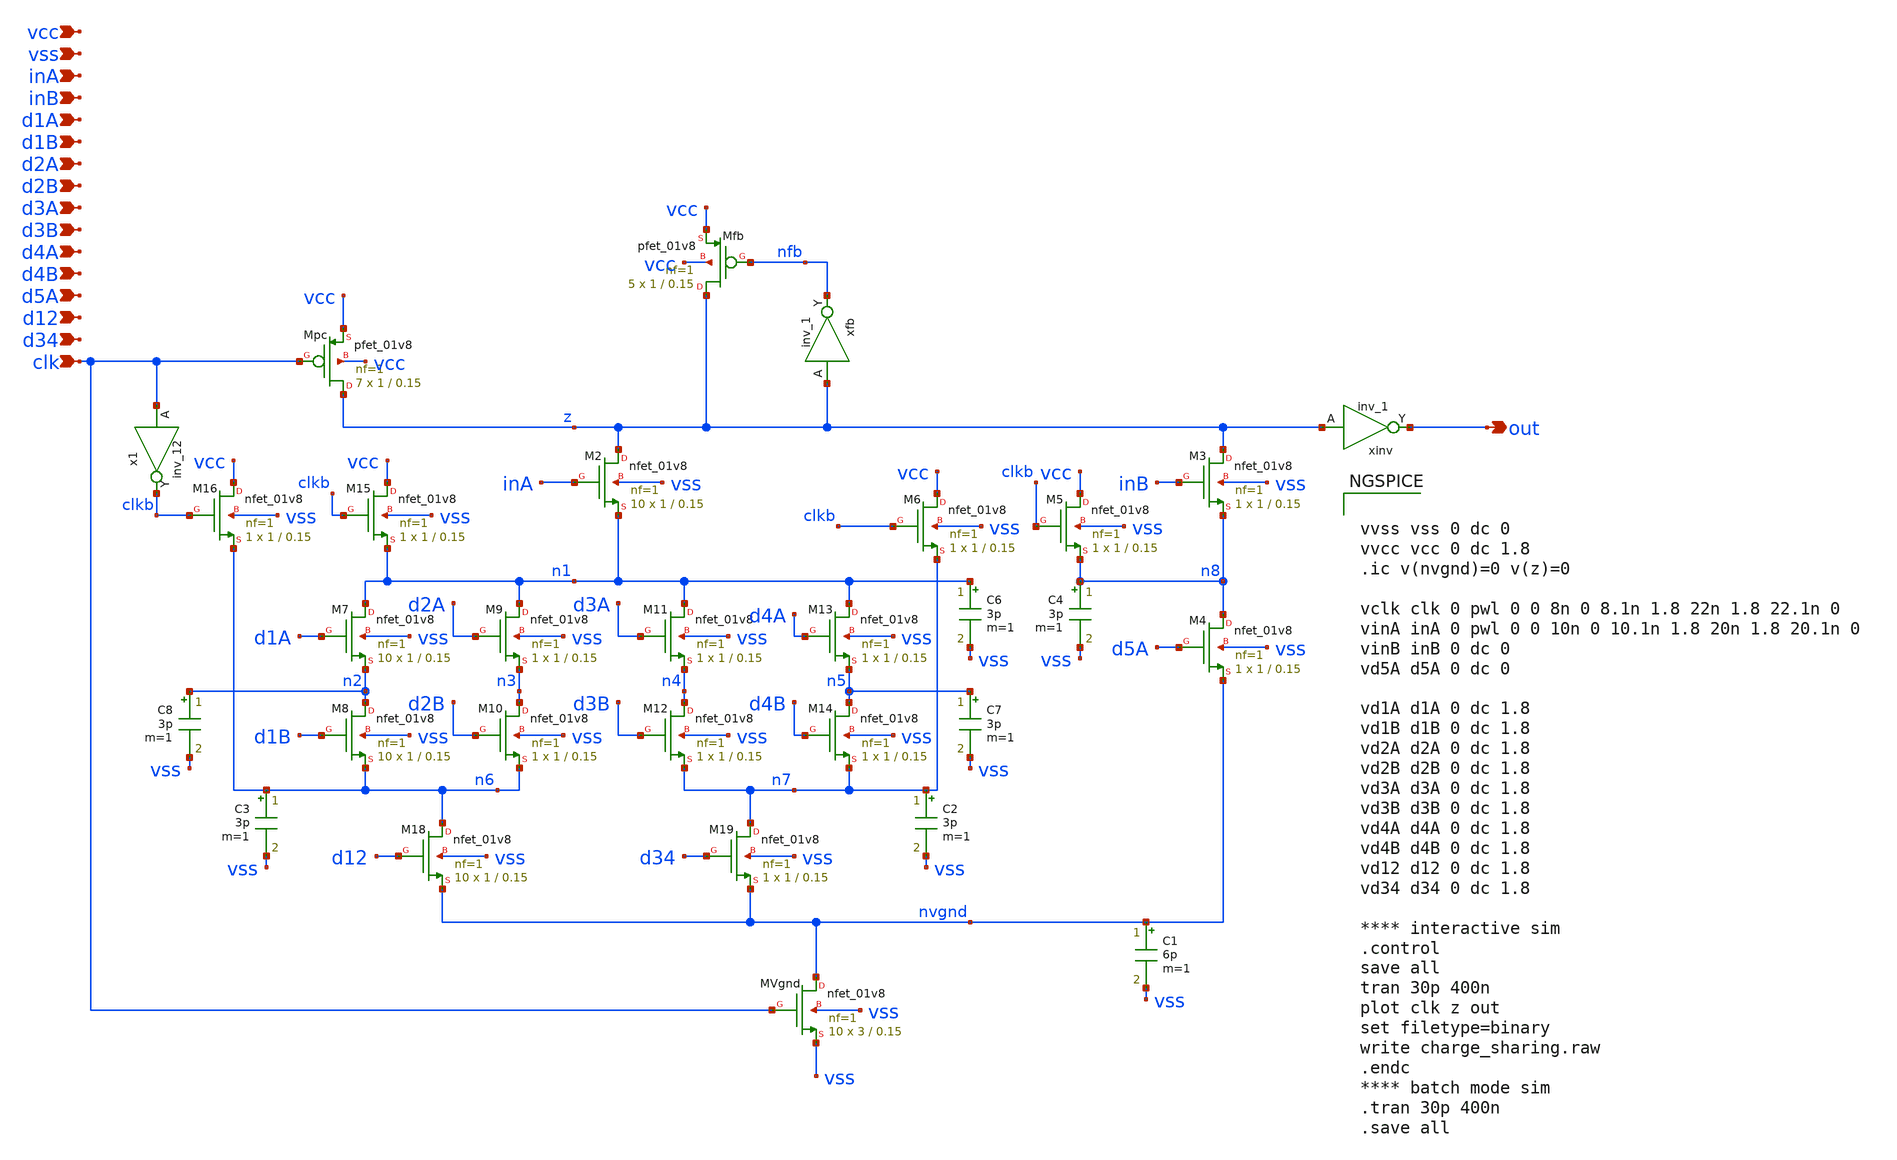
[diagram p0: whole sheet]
** sch_path: src/xe/test_cases/charge_sharing.sch
**.subckt charge_sharing clk out d5A d4B d4A d3B d3A d2B d2A d1B d1A inB inA d34 d12 vss vcc
*.ipin clk
*.opin out
*.ipin d5A
*.ipin d4B
*.ipin d4A
*.ipin d3B
*.ipin d3A
*.ipin d2B
*.ipin d2A
*.ipin d1B
*.ipin d1A
*.ipin inB
*.ipin inA
*.ipin d34
*.ipin d12
*.ipin vss
*.ipin vcc
XMpc z clk vcc vcc sky130_fd_pr__pfet_01v8 L=0.15 W=1 nf=1 ad='int((nf+1)/2) * W/nf * 0.29' as='int((nf+2)/2) * W/nf * 0.29'
+ pd='2*int((nf+1)/2) * (W/nf + 0.29)' ps='2*int((nf+2)/2) * (W/nf + 0.29)' nrd='0.29 / W' nrs='0.29 / W'
+ sa=0 sb=0 sd=0 mult=7 m=7
XM2 z inA n1 vss sky130_fd_pr__nfet_01v8 L=0.15 W=1 nf=1 ad='int((nf+1)/2) * W/nf * 0.29' as='int((nf+2)/2) * W/nf * 0.29'
+ pd='2*int((nf+1)/2) * (W/nf + 0.29)' ps='2*int((nf+2)/2) * (W/nf + 0.29)' nrd='0.29 / W' nrs='0.29 / W'
+ sa=0 sb=0 sd=0 mult=10 m=10
xfb z vss vss vcc vcc nfb sky130_fd_sc_hd__inv_1
xinv z vss vss vcc vcc out sky130_fd_sc_hd__inv_1
XM3 z inB n8 vss sky130_fd_pr__nfet_01v8 L=0.15 W=1 nf=1 ad='int((nf+1)/2) * W/nf * 0.29' as='int((nf+2)/2) * W/nf * 0.29'
+ pd='2*int((nf+1)/2) * (W/nf + 0.29)' ps='2*int((nf+2)/2) * (W/nf + 0.29)' nrd='0.29 / W' nrs='0.29 / W'
+ sa=0 sb=0 sd=0 mult=1 m=1
XM4 n8 d5A nvgnd vss sky130_fd_pr__nfet_01v8 L=0.15 W=1 nf=1 ad='int((nf+1)/2) * W/nf * 0.29' as='int((nf+2)/2) * W/nf * 0.29'
+ pd='2*int((nf+1)/2) * (W/nf + 0.29)' ps='2*int((nf+2)/2) * (W/nf + 0.29)' nrd='0.29 / W' nrs='0.29 / W'
+ sa=0 sb=0 sd=0 mult=1 m=1
XM5 vcc clkb n8 vss sky130_fd_pr__nfet_01v8 L=0.15 W=1 nf=1 ad='int((nf+1)/2) * W/nf * 0.29' as='int((nf+2)/2) * W/nf * 0.29'
+ pd='2*int((nf+1)/2) * (W/nf + 0.29)' ps='2*int((nf+2)/2) * (W/nf + 0.29)' nrd='0.29 / W' nrs='0.29 / W'
+ sa=0 sb=0 sd=0 mult=1 m=1
XM6 vcc clkb n7 vss sky130_fd_pr__nfet_01v8 L=0.15 W=1 nf=1 ad='int((nf+1)/2) * W/nf * 0.29' as='int((nf+2)/2) * W/nf * 0.29'
+ pd='2*int((nf+1)/2) * (W/nf + 0.29)' ps='2*int((nf+2)/2) * (W/nf + 0.29)' nrd='0.29 / W' nrs='0.29 / W'
+ sa=0 sb=0 sd=0 mult=1 m=1
XM7 n1 d1A n2 vss sky130_fd_pr__nfet_01v8 L=0.15 W=1 nf=1 ad='int((nf+1)/2) * W/nf * 0.29' as='int((nf+2)/2) * W/nf * 0.29'
+ pd='2*int((nf+1)/2) * (W/nf + 0.29)' ps='2*int((nf+2)/2) * (W/nf + 0.29)' nrd='0.29 / W' nrs='0.29 / W'
+ sa=0 sb=0 sd=0 mult=10 m=10
XM8 n2 d1B n6 vss sky130_fd_pr__nfet_01v8 L=0.15 W=1 nf=1 ad='int((nf+1)/2) * W/nf * 0.29' as='int((nf+2)/2) * W/nf * 0.29'
+ pd='2*int((nf+1)/2) * (W/nf + 0.29)' ps='2*int((nf+2)/2) * (W/nf + 0.29)' nrd='0.29 / W' nrs='0.29 / W'
+ sa=0 sb=0 sd=0 mult=10 m=10
XM9 n1 d2A n3 vss sky130_fd_pr__nfet_01v8 L=0.15 W=1 nf=1 ad='int((nf+1)/2) * W/nf * 0.29' as='int((nf+2)/2) * W/nf * 0.29'
+ pd='2*int((nf+1)/2) * (W/nf + 0.29)' ps='2*int((nf+2)/2) * (W/nf + 0.29)' nrd='0.29 / W' nrs='0.29 / W'
+ sa=0 sb=0 sd=0 mult=1 m=1
XM10 n3 d2B n6 vss sky130_fd_pr__nfet_01v8 L=0.15 W=1 nf=1 ad='int((nf+1)/2) * W/nf * 0.29' as='int((nf+2)/2) * W/nf * 0.29'
+ pd='2*int((nf+1)/2) * (W/nf + 0.29)' ps='2*int((nf+2)/2) * (W/nf + 0.29)' nrd='0.29 / W' nrs='0.29 / W'
+ sa=0 sb=0 sd=0 mult=1 m=1
XM11 n1 d3A n4 vss sky130_fd_pr__nfet_01v8 L=0.15 W=1 nf=1 ad='int((nf+1)/2) * W/nf * 0.29' as='int((nf+2)/2) * W/nf * 0.29'
+ pd='2*int((nf+1)/2) * (W/nf + 0.29)' ps='2*int((nf+2)/2) * (W/nf + 0.29)' nrd='0.29 / W' nrs='0.29 / W'
+ sa=0 sb=0 sd=0 mult=1 m=1
XM12 n4 d3B n7 vss sky130_fd_pr__nfet_01v8 L=0.15 W=1 nf=1 ad='int((nf+1)/2) * W/nf * 0.29' as='int((nf+2)/2) * W/nf * 0.29'
+ pd='2*int((nf+1)/2) * (W/nf + 0.29)' ps='2*int((nf+2)/2) * (W/nf + 0.29)' nrd='0.29 / W' nrs='0.29 / W'
+ sa=0 sb=0 sd=0 mult=1 m=1
XM13 n1 d4A n5 vss sky130_fd_pr__nfet_01v8 L=0.15 W=1 nf=1 ad='int((nf+1)/2) * W/nf * 0.29' as='int((nf+2)/2) * W/nf * 0.29'
+ pd='2*int((nf+1)/2) * (W/nf + 0.29)' ps='2*int((nf+2)/2) * (W/nf + 0.29)' nrd='0.29 / W' nrs='0.29 / W'
+ sa=0 sb=0 sd=0 mult=1 m=1
XM14 n5 d4B n7 vss sky130_fd_pr__nfet_01v8 L=0.15 W=1 nf=1 ad='int((nf+1)/2) * W/nf * 0.29' as='int((nf+2)/2) * W/nf * 0.29'
+ pd='2*int((nf+1)/2) * (W/nf + 0.29)' ps='2*int((nf+2)/2) * (W/nf + 0.29)' nrd='0.29 / W' nrs='0.29 / W'
+ sa=0 sb=0 sd=0 mult=1 m=1
XM15 vcc clkb n1 vss sky130_fd_pr__nfet_01v8 L=0.15 W=1 nf=1 ad='int((nf+1)/2) * W/nf * 0.29' as='int((nf+2)/2) * W/nf * 0.29'
+ pd='2*int((nf+1)/2) * (W/nf + 0.29)' ps='2*int((nf+2)/2) * (W/nf + 0.29)' nrd='0.29 / W' nrs='0.29 / W'
+ sa=0 sb=0 sd=0 mult=1 m=1
XM16 vcc clkb n6 vss sky130_fd_pr__nfet_01v8 L=0.15 W=1 nf=1 ad='int((nf+1)/2) * W/nf * 0.29' as='int((nf+2)/2) * W/nf * 0.29'
+ pd='2*int((nf+1)/2) * (W/nf + 0.29)' ps='2*int((nf+2)/2) * (W/nf + 0.29)' nrd='0.29 / W' nrs='0.29 / W'
+ sa=0 sb=0 sd=0 mult=1 m=1
XMVgnd nvgnd clk vss vss sky130_fd_pr__nfet_01v8 L=0.15 W=3 nf=1 ad='int((nf+1)/2) * W/nf * 0.29' as='int((nf+2)/2) * W/nf * 0.29'
+ pd='2*int((nf+1)/2) * (W/nf + 0.29)' ps='2*int((nf+2)/2) * (W/nf + 0.29)' nrd='0.29 / W' nrs='0.29 / W'
+ sa=0 sb=0 sd=0 mult=10 m=10
XM18 n6 d12 nvgnd vss sky130_fd_pr__nfet_01v8 L=0.15 W=1 nf=1 ad='int((nf+1)/2) * W/nf * 0.29' as='int((nf+2)/2) * W/nf * 0.29'
+ pd='2*int((nf+1)/2) * (W/nf + 0.29)' ps='2*int((nf+2)/2) * (W/nf + 0.29)' nrd='0.29 / W' nrs='0.29 / W'
+ sa=0 sb=0 sd=0 mult=10 m=10
XM19 n7 d34 nvgnd vss sky130_fd_pr__nfet_01v8 L=0.15 W=1 nf=1 ad='int((nf+1)/2) * W/nf * 0.29' as='int((nf+2)/2) * W/nf * 0.29'
+ pd='2*int((nf+1)/2) * (W/nf + 0.29)' ps='2*int((nf+2)/2) * (W/nf + 0.29)' nrd='0.29 / W' nrs='0.29 / W'
+ sa=0 sb=0 sd=0 mult=1 m=1
XMfb z nfb vcc vcc sky130_fd_pr__pfet_01v8 L=0.15 W=1 nf=1 ad='int((nf+1)/2) * W/nf * 0.29' as='int((nf+2)/2) * W/nf * 0.29'
+ pd='2*int((nf+1)/2) * (W/nf + 0.29)' ps='2*int((nf+2)/2) * (W/nf + 0.29)' nrd='0.29 / W' nrs='0.29 / W'
+ sa=0 sb=0 sd=0 mult=5 m=5
x1 clk vss vss vcc vcc clkb sky130_fd_sc_hd__inv_12
C1 nvgnd vss 6p m=1
C2 n7 vss 3p m=1
C3 n6 vss 3p m=1
C4 n8 vss 3p m=1
C6 n1 vss 3p m=1
C7 n5 vss 3p m=1
C8 n2 vss 3p m=1
**** begin user architecture code


vvss vss 0 dc 0
vvcc vcc 0 dc 1.8
.ic v(nvgnd)=0 v(z)=0

vclk clk 0 pwl 0 0 8n 0 8.1n 1.8 22n 1.8 22.1n 0
vinA inA 0 pwl 0 0 10n 0 10.1n 1.8 20n 1.8 20.1n 0
vinB inB 0 dc 0
vd5A d5A 0 dc 0

vd1A d1A 0 dc 1.8
vd1B d1B 0 dc 1.8
vd2A d2A 0 dc 1.8
vd2B d2B 0 dc 1.8
vd3A d3A 0 dc 1.8
vd3B d3B 0 dc 1.8
vd4A d4A 0 dc 1.8
vd4B d4B 0 dc 1.8
vd12 d12 0 dc 1.8
vd34 d34 0 dc 1.8

**** interactive sim
.control
save all
tran 30p 400n
plot clk z out
set filetype=binary
write charge_sharing.raw
.endc
**** batch mode sim
.tran 30p 400n
.save all




** opencircuitdesign pdks install
.lib $::SKYWATER_MODELS/sky130.lib.spice tt
.include $::SKYWATER_STDCELLS/sky130_fd_sc_hd.spice


**** end user architecture code
**.ends
.end
